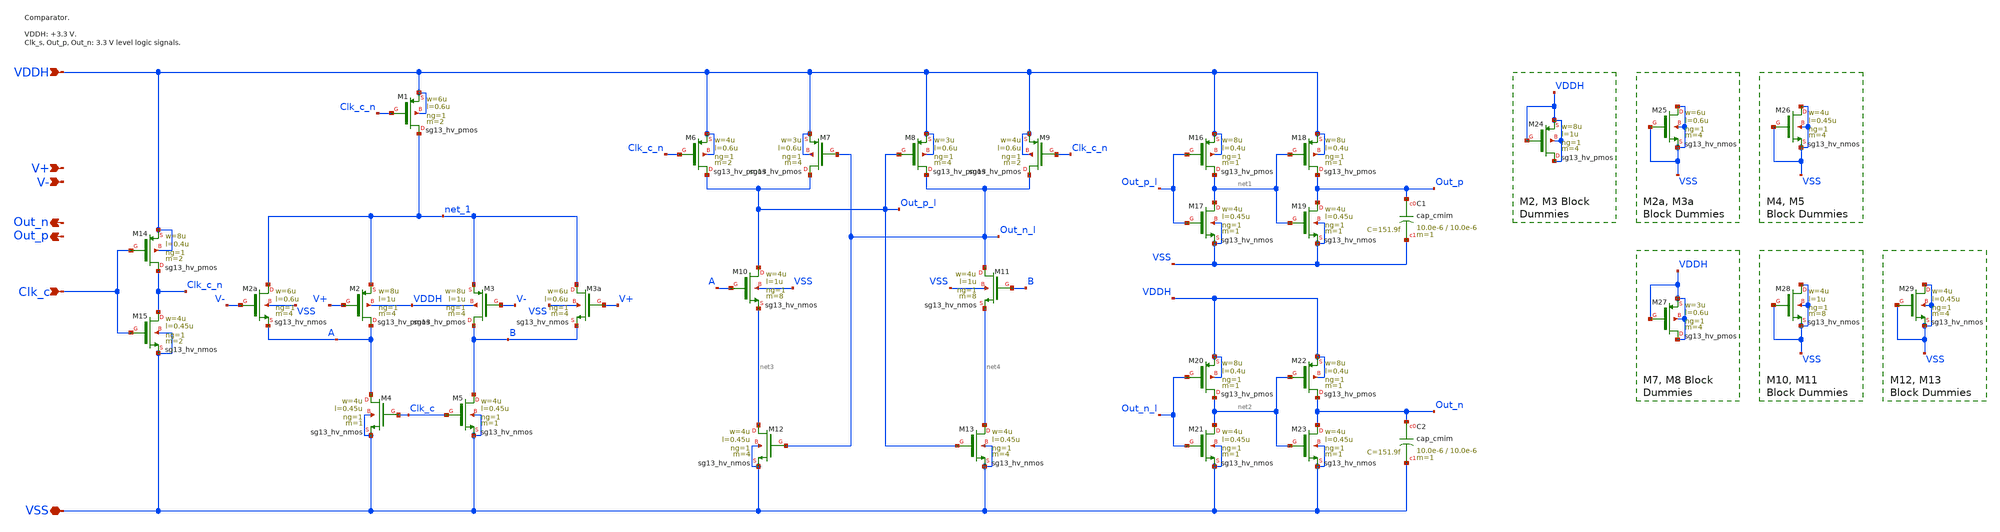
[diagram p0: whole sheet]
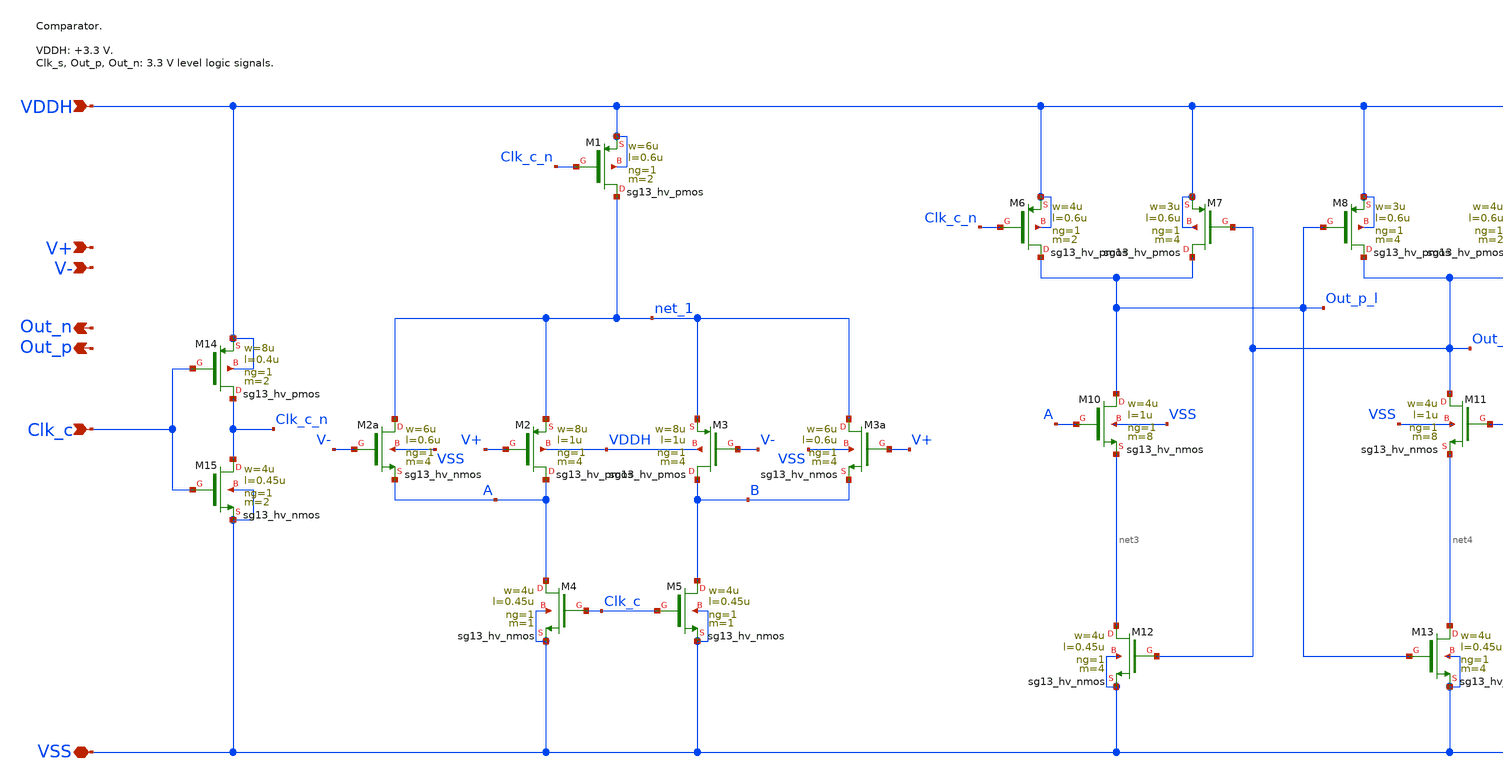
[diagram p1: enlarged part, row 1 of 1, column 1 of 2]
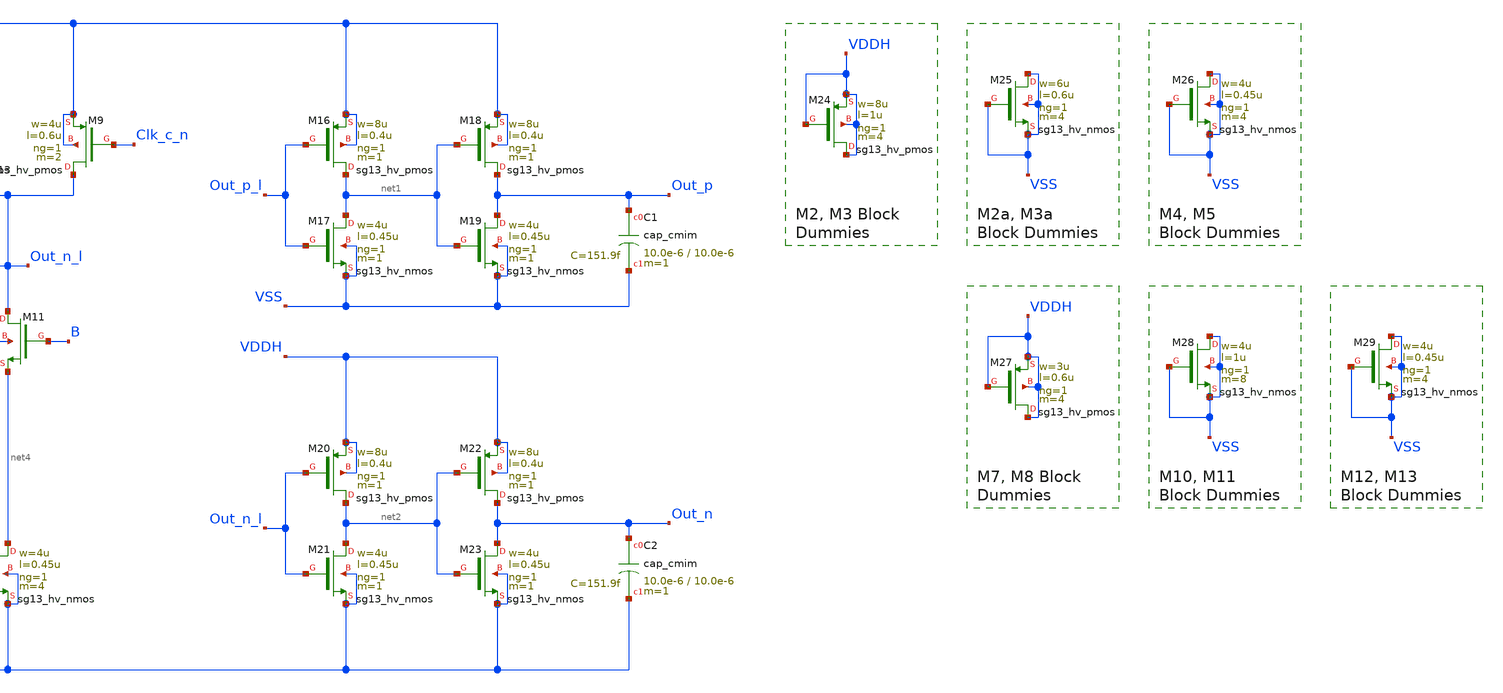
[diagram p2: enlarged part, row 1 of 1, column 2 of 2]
** sch_path: comparator_300mhz/xschem/comparator.sch
**.subckt comparator Clk_c VSS VDDH V+ V- Out_p Out_n
*.ipin Clk_c
*.iopin VSS
*.ipin VDDH
*.ipin V+
*.ipin V-
*.opin Out_p
*.opin Out_n
XM14 Clk_c_n Clk_c VDDH VDDH sg13_hv_pmos w=8u l=0.4u ng=1 m=2 mm_ok=1
XM15 Clk_c_n Clk_c VSS VSS sg13_hv_nmos w=4u l=0.45u ng=1 m=2 mm_ok=1
XM1 net_1 Clk_c_n VDDH VDDH sg13_hv_pmos w=6u l=0.6u ng=1 m=2 mm_ok=1
XM2 A V+ net_1 VDDH sg13_hv_pmos w=8u l=1u ng=1 m=4 mm_ok=1
XM3 B V- net_1 VDDH sg13_hv_pmos w=8u l=1u ng=1 m=4 mm_ok=1
XM2a net_1 V- A VSS sg13_hv_nmos w=6u l=0.6u ng=1 m=4 mm_ok=1
XM3a net_1 V+ B VSS sg13_hv_nmos w=6u l=0.6u ng=1 m=4 mm_ok=1
XM4 A Clk_c VSS VSS sg13_hv_nmos w=4u l=0.45u ng=1 m=1 mm_ok=1
XM5 B Clk_c VSS VSS sg13_hv_nmos w=4u l=0.45u ng=1 m=1 mm_ok=1
XM6 Out_p_l Clk_c_n VDDH VDDH sg13_hv_pmos w=4u l=0.6u ng=1 m=2 mm_ok=1
XM7 Out_p_l Out_n_l VDDH VDDH sg13_hv_pmos w=3u l=0.6u ng=1 m=4 mm_ok=1
XM8 Out_n_l Out_p_l VDDH VDDH sg13_hv_pmos w=3u l=0.6u ng=1 m=4 mm_ok=1
XM9 Out_n_l Clk_c_n VDDH VDDH sg13_hv_pmos w=4u l=0.6u ng=1 m=2 mm_ok=1
XM10 Out_p_l A net3 VSS sg13_hv_nmos w=4u l=1u ng=1 m=8 mm_ok=1
XM11 Out_n_l B net4 VSS sg13_hv_nmos w=4u l=1u ng=1 m=8 mm_ok=1
XM12 net3 Out_n_l VSS VSS sg13_hv_nmos w=4u l=0.45u ng=1 m=4 mm_ok=1
XM13 net4 Out_p_l VSS VSS sg13_hv_nmos w=4u l=0.45u ng=1 m=4 mm_ok=1
XM16 net1 Out_p_l VDDH VDDH sg13_hv_pmos w=8u l=0.4u ng=1 m=1 mm_ok=1
XM17 net1 Out_p_l VSS VSS sg13_hv_nmos w=4u l=0.45u ng=1 m=1 mm_ok=1
XM18 Out_p net1 VDDH VDDH sg13_hv_pmos w=8u l=0.4u ng=1 m=1 mm_ok=1
XM19 Out_p net1 VSS VSS sg13_hv_nmos w=4u l=0.45u ng=1 m=1 mm_ok=1
XM20 net2 Out_n_l VDDH VDDH sg13_hv_pmos w=8u l=0.4u ng=1 m=1 mm_ok=1
XM21 net2 Out_n_l VSS VSS sg13_hv_nmos w=4u l=0.45u ng=1 m=1 mm_ok=1
XM22 Out_n net2 VDDH VDDH sg13_hv_pmos w=8u l=0.4u ng=1 m=1 mm_ok=1
XM23 Out_n net2 VSS VSS sg13_hv_nmos w=4u l=0.45u ng=1 m=1 mm_ok=1
XC1 Out_p VSS cap_cmim w=10.0e-6 l=10.0e-6 m=1 mm_ok=1
XC2 Out_n VSS cap_cmim w=10.0e-6 l=10.0e-6 m=1 mm_ok=1
XM24 VDDH VDDH VDDH VDDH sg13_hv_pmos w=8u l=1u ng=1 m=4 mm_ok=1
XM25 VSS VSS VSS VSS sg13_hv_nmos w=6u l=0.6u ng=1 m=4 mm_ok=1
XM26 VSS VSS VSS VSS sg13_hv_nmos w=4u l=0.45u ng=1 m=4 mm_ok=1
XM27 VDDH VDDH VDDH VDDH sg13_hv_pmos w=3u l=0.6u ng=1 m=4 mm_ok=1
XM28 VSS VSS VSS VSS sg13_hv_nmos w=4u l=1u ng=1 m=8 mm_ok=1
XM29 VSS VSS VSS VSS sg13_hv_nmos w=4u l=0.45u ng=1 m=4 mm_ok=1
**.ends
.end
